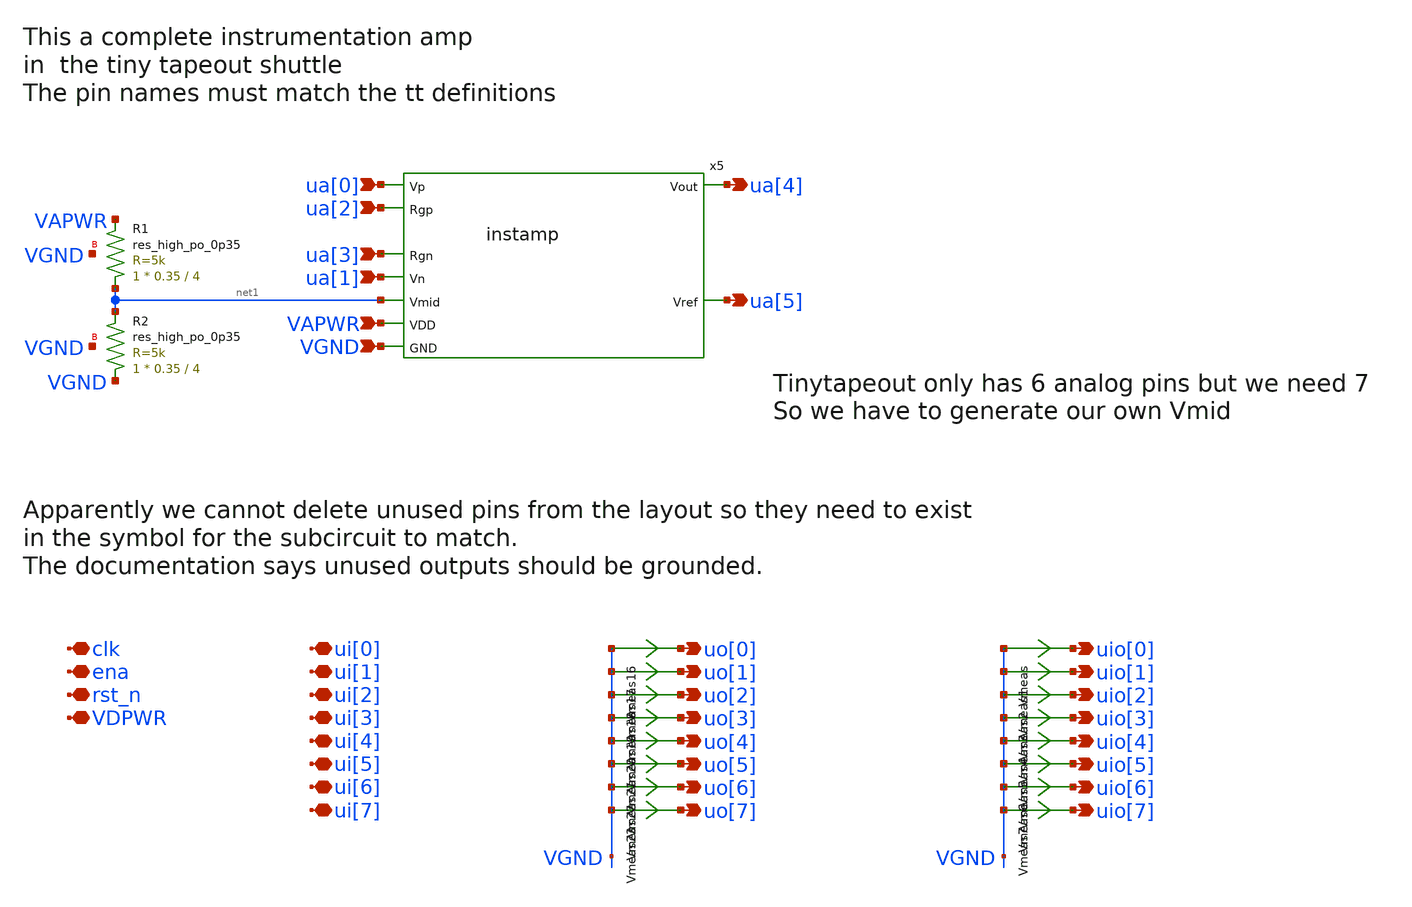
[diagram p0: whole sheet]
** sch_path: xschem/tt_um_jonathanwest3_instamp_sp2026.sch
* Copyright 2021 Stefan Frederik Schippers
* Licensed under the Apache License, Version 2.0 (the "License");
* you may not use this file except in compliance with the License.
* You may obtain a copy of the License at
* https://www.apache.org/licenses/LICENSE-2.0
* Unless required by applicable law or agreed to in writing, software
* distributed under the License is distributed on an "AS IS" BASIS,
* WITHOUT WARRANTIES OR CONDITIONS OF ANY KIND, either express or implied.
* See the License for the specific language governing permissions and
* limitations under the License.
**.subckt tt_um_jonathanwest3_instamp_sp2026 ua[0] ua[1] ua[4] ua[5] ua[2] ua[3] VGND VAPWR uo[0]
*+ uo[1] uo[2] uo[3] uo[4] uo[5] uo[6] uo[7] uio[0] uio[1] uio[2] uio[3] uio[4] uio[5] uio[6] uio[7] ui[0]
*+ ui[1] ui[2] ui[3] ui[4] ui[5] ui[6] ui[7] clk ena rst_n VDPWR
*.ipin ua[0]
*.ipin ua[1]
*.opin ua[4]
*.opin ua[5]
*.ipin ua[2]
*.ipin ua[3]
*.ipin VGND
*.ipin VAPWR
*.opin uo[0]
*.opin uo[1]
*.opin uo[2]
*.opin uo[3]
*.opin uo[4]
*.opin uo[5]
*.opin uo[6]
*.opin uo[7]
*.opin uio[0]
*.opin uio[1]
*.opin uio[2]
*.opin uio[3]
*.opin uio[4]
*.opin uio[5]
*.opin uio[6]
*.opin uio[7]
*.iopin ui[0]
*.iopin ui[1]
*.iopin ui[2]
*.iopin ui[3]
*.iopin ui[4]
*.iopin ui[5]
*.iopin ui[6]
*.iopin ui[7]
*.iopin clk
*.iopin ena
*.iopin rst_n
*.iopin VDPWR
x5 ua[1] ua[3] ua[0] ua[2] net1 ua[4] ua[5] VAPWR VGND instamp
XR1 net1 VAPWR VGND sky130_fd_pr__res_high_po_0p35 L=4 mult=1 m=1
XR2 VGND net1 VGND sky130_fd_pr__res_high_po_0p35 L=4 mult=1 m=1
Vmeas VGND uio[0] 0
.save i(vmeas)
Vmeas1 VGND uio[1] 0
.save i(vmeas1)
Vmeas2 VGND uio[2] 0
.save i(vmeas2)
Vmeas3 VGND uio[3] 0
.save i(vmeas3)
Vmeas4 VGND uio[4] 0
.save i(vmeas4)
Vmeas5 VGND uio[5] 0
.save i(vmeas5)
Vmeas6 VGND uio[6] 0
.save i(vmeas6)
Vmeas7 VGND uio[7] 0
.save i(vmeas7)
Vmeas16 VGND uo[0] 0
.save i(vmeas16)
Vmeas17 VGND uo[1] 0
.save i(vmeas17)
Vmeas18 VGND uo[2] 0
.save i(vmeas18)
Vmeas19 VGND uo[3] 0
.save i(vmeas19)
Vmeas20 VGND uo[4] 0
.save i(vmeas20)
Vmeas21 VGND uo[5] 0
.save i(vmeas21)
Vmeas22 VGND uo[6] 0
.save i(vmeas22)
Vmeas23 VGND uo[7] 0
.save i(vmeas23)
**.ends
.end
